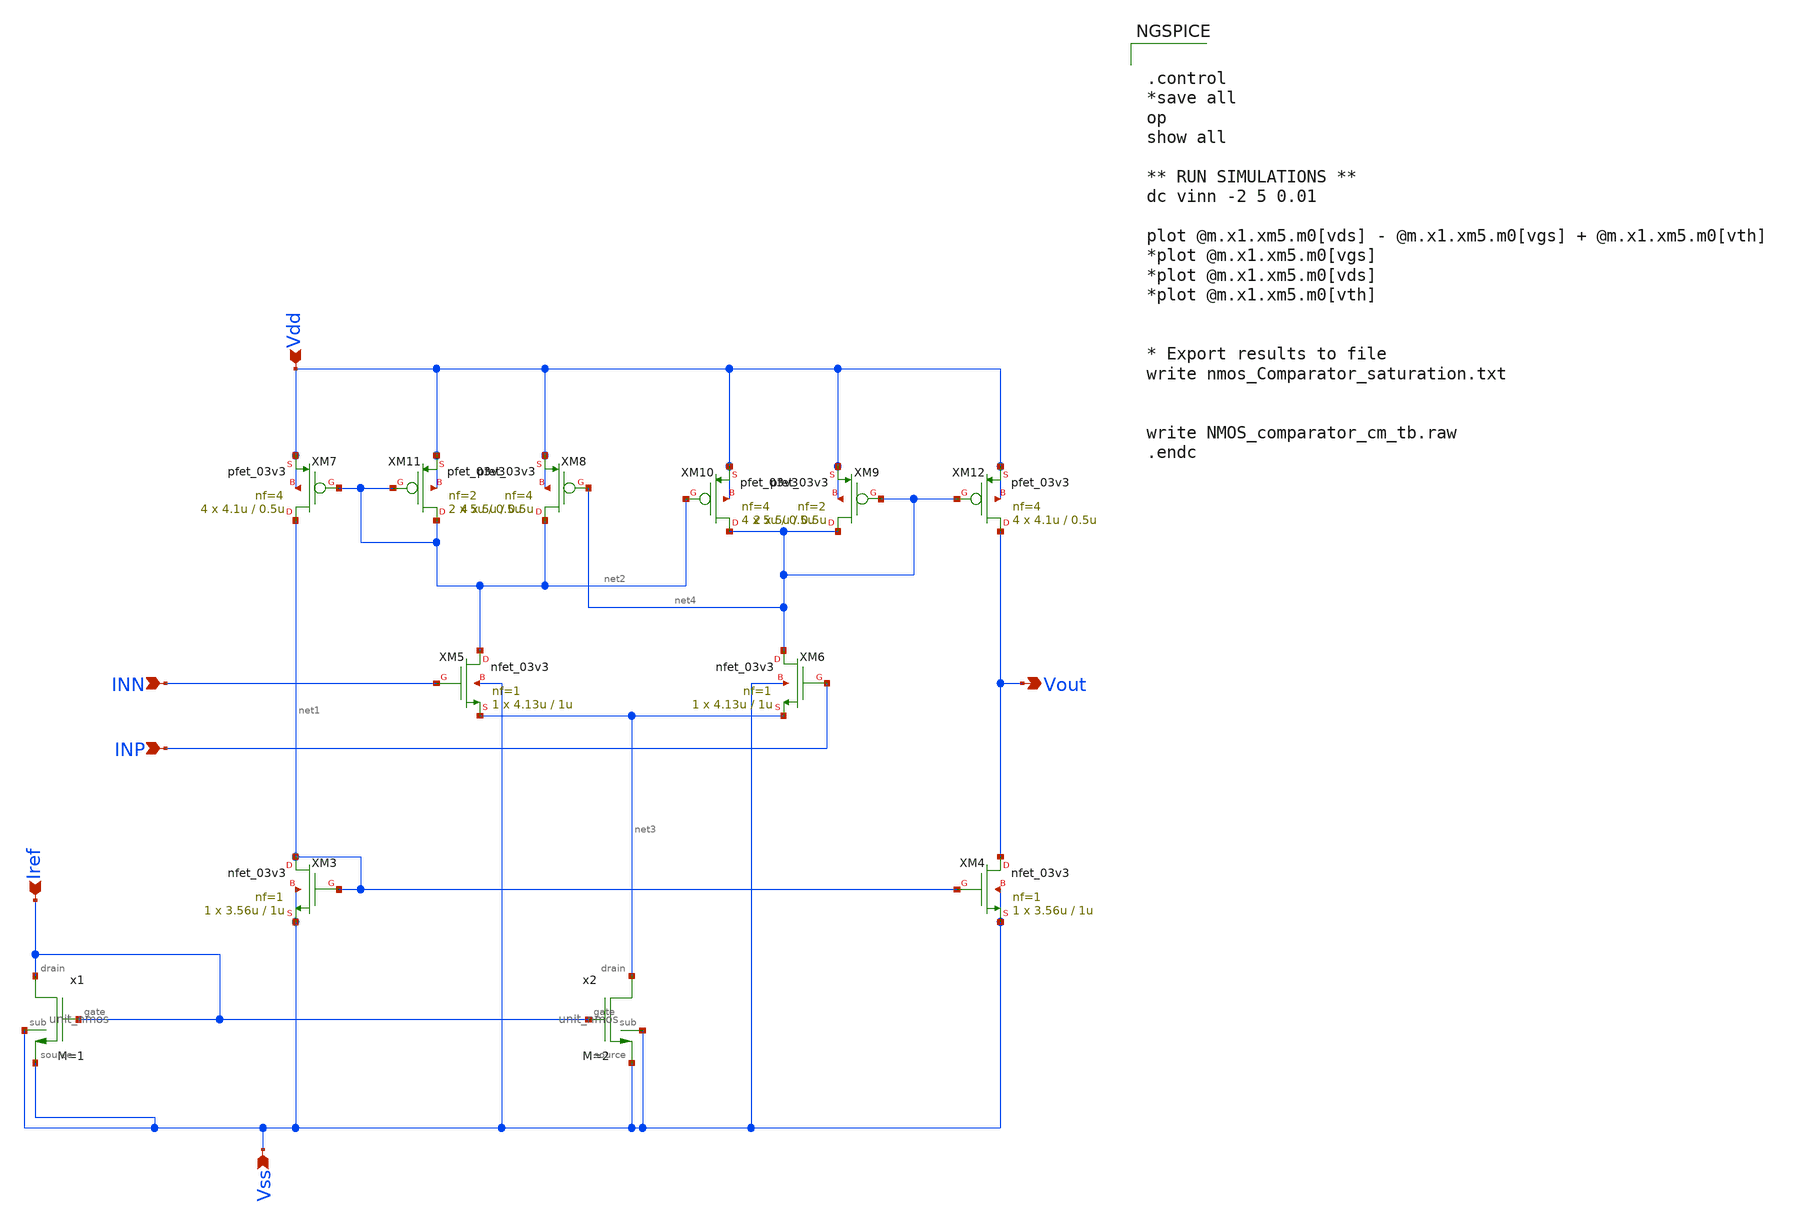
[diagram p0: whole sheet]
** sch_path: designs/libs/core_analog/Comparator/Nmos_Comparator.sch
**.subckt Nmos_Comparator Vss Vdd Iref INN INP Vout
*.ipin Vss
*.ipin Vdd
*.ipin Iref
*.ipin INN
*.ipin INP
*.opin Vout
XM3 net1 net1 Vss Vss nfet_03v3 L=1u W=3.56u nf=1 ad='int((nf+1)/2) * W/nf * 0.18u' as='int((nf+2)/2) * W/nf * 0.18u'
+ pd='2*int((nf+1)/2) * (W/nf + 0.18u)' ps='2*int((nf+2)/2) * (W/nf + 0.18u)' nrd='0.18u / W' nrs='0.18u / W'
+ sa=0 sb=0 sd=0 m=1
XM4 Vout net1 Vss Vss nfet_03v3 L=1u W=3.56u nf=1 ad='int((nf+1)/2) * W/nf * 0.18u' as='int((nf+2)/2) * W/nf * 0.18u'
+ pd='2*int((nf+1)/2) * (W/nf + 0.18u)' ps='2*int((nf+2)/2) * (W/nf + 0.18u)' nrd='0.18u / W' nrs='0.18u / W'
+ sa=0 sb=0 sd=0 m=1
XM5 net2 INN net3 Vss nfet_03v3 L=1u W=4.13u nf=1 ad='int((nf+1)/2) * W/nf * 0.18u' as='int((nf+2)/2) * W/nf * 0.18u'
+ pd='2*int((nf+1)/2) * (W/nf + 0.18u)' ps='2*int((nf+2)/2) * (W/nf + 0.18u)' nrd='0.18u / W' nrs='0.18u / W'
+ sa=0 sb=0 sd=0 m=1
XM6 net4 INP net3 Vss nfet_03v3 L=1u W=4.13u nf=1 ad='int((nf+1)/2) * W/nf * 0.18u' as='int((nf+2)/2) * W/nf * 0.18u'
+ pd='2*int((nf+1)/2) * (W/nf + 0.18u)' ps='2*int((nf+2)/2) * (W/nf + 0.18u)' nrd='0.18u / W' nrs='0.18u / W'
+ sa=0 sb=0 sd=0 m=1
XM7 net1 net2 Vdd Vdd pfet_03v3 L=0.5u W=4.1u nf=4 ad='int((nf+1)/2) * W/nf * 0.18u' as='int((nf+2)/2) * W/nf * 0.18u'
+ pd='2*int((nf+1)/2) * (W/nf + 0.18u)' ps='2*int((nf+2)/2) * (W/nf + 0.18u)' nrd='0.18u / W' nrs='0.18u / W'
+ sa=0 sb=0 sd=0 m=4
XM8 net2 net4 Vdd Vdd pfet_03v3 L=0.5u W=5u nf=4 ad='int((nf+1)/2) * W/nf * 0.18u' as='int((nf+2)/2) * W/nf * 0.18u'
+ pd='2*int((nf+1)/2) * (W/nf + 0.18u)' ps='2*int((nf+2)/2) * (W/nf + 0.18u)' nrd='0.18u / W' nrs='0.18u / W'
+ sa=0 sb=0 sd=0 m=4
XM9 net4 net4 Vdd Vdd pfet_03v3 L=0.5u W=5u nf=2 ad='int((nf+1)/2) * W/nf * 0.18u' as='int((nf+2)/2) * W/nf * 0.18u'
+ pd='2*int((nf+1)/2) * (W/nf + 0.18u)' ps='2*int((nf+2)/2) * (W/nf + 0.18u)' nrd='0.18u / W' nrs='0.18u / W'
+ sa=0 sb=0 sd=0 m=2
XM10 net4 net2 Vdd Vdd pfet_03v3 L=0.5u W=5u nf=4 ad='int((nf+1)/2) * W/nf * 0.18u' as='int((nf+2)/2) * W/nf * 0.18u'
+ pd='2*int((nf+1)/2) * (W/nf + 0.18u)' ps='2*int((nf+2)/2) * (W/nf + 0.18u)' nrd='0.18u / W' nrs='0.18u / W'
+ sa=0 sb=0 sd=0 m=4
XM11 net2 net2 Vdd Vdd pfet_03v3 L=0.5u W=5u nf=2 ad='int((nf+1)/2) * W/nf * 0.18u' as='int((nf+2)/2) * W/nf * 0.18u'
+ pd='2*int((nf+1)/2) * (W/nf + 0.18u)' ps='2*int((nf+2)/2) * (W/nf + 0.18u)' nrd='0.18u / W' nrs='0.18u / W'
+ sa=0 sb=0 sd=0 m=2
XM12 Vout net4 Vdd Vdd pfet_03v3 L=0.5u W=4.1u nf=4 ad='int((nf+1)/2) * W/nf * 0.18u' as='int((nf+2)/2) * W/nf * 0.18u'
+ pd='2*int((nf+1)/2) * (W/nf + 0.18u)' ps='2*int((nf+2)/2) * (W/nf + 0.18u)' nrd='0.18u / W' nrs='0.18u / W'
+ sa=0 sb=0 sd=0 m=4
x1 Iref Vss Iref Vss unit_nmos M=1
x2 net3 Vss Iref Vss unit_nmos M=2
**** begin user architecture code


.control
*save all
op
show all

** RUN SIMULATIONS **
dc vinn -2 5 0.01

plot @m.x1.xm5.m0[vds] - @m.x1.xm5.m0[vgs] + @m.x1.xm5.m0[vth]
*plot @m.x1.xm5.m0[vgs]
*plot @m.x1.xm5.m0[vds]
*plot @m.x1.xm5.m0[vth]


* Export results to file
write nmos_Comparator_saturation.txt


write NMOS_comparator_cm_tb.raw
.endc


**** end user architecture code
**.ends

* expanding   symbol:  libs/core_analog/unit_nmos/unit_nmos.sym # of pins=4
** sym_path: libs/core_analog/unit_nmos/unit_nmos.sym
** sch_path: libs/core_analog/unit_nmos/unit_nmos.sch
.subckt unit_nmos drain sub gate source
*.iopin drain
*.iopin source
*.iopin sub
*.iopin gate
XM1 drain gate source sub nfet_03v3 L=1u W=2.5u nf=1 ad='int((nf+1)/2) * W/nf * 0.18u' as='int((nf+2)/2) * W/nf * 0.18u'
+ pd='2*int((nf+1)/2) * (W/nf + 0.18u)' ps='2*int((nf+2)/2) * (W/nf + 0.18u)' nrd='0.18u / W' nrs='0.18u / W'
+ sa=0 sb=0 sd=0 m={M}
**** begin user architecture code

.param M=1

**** end user architecture code
.ends

.end
